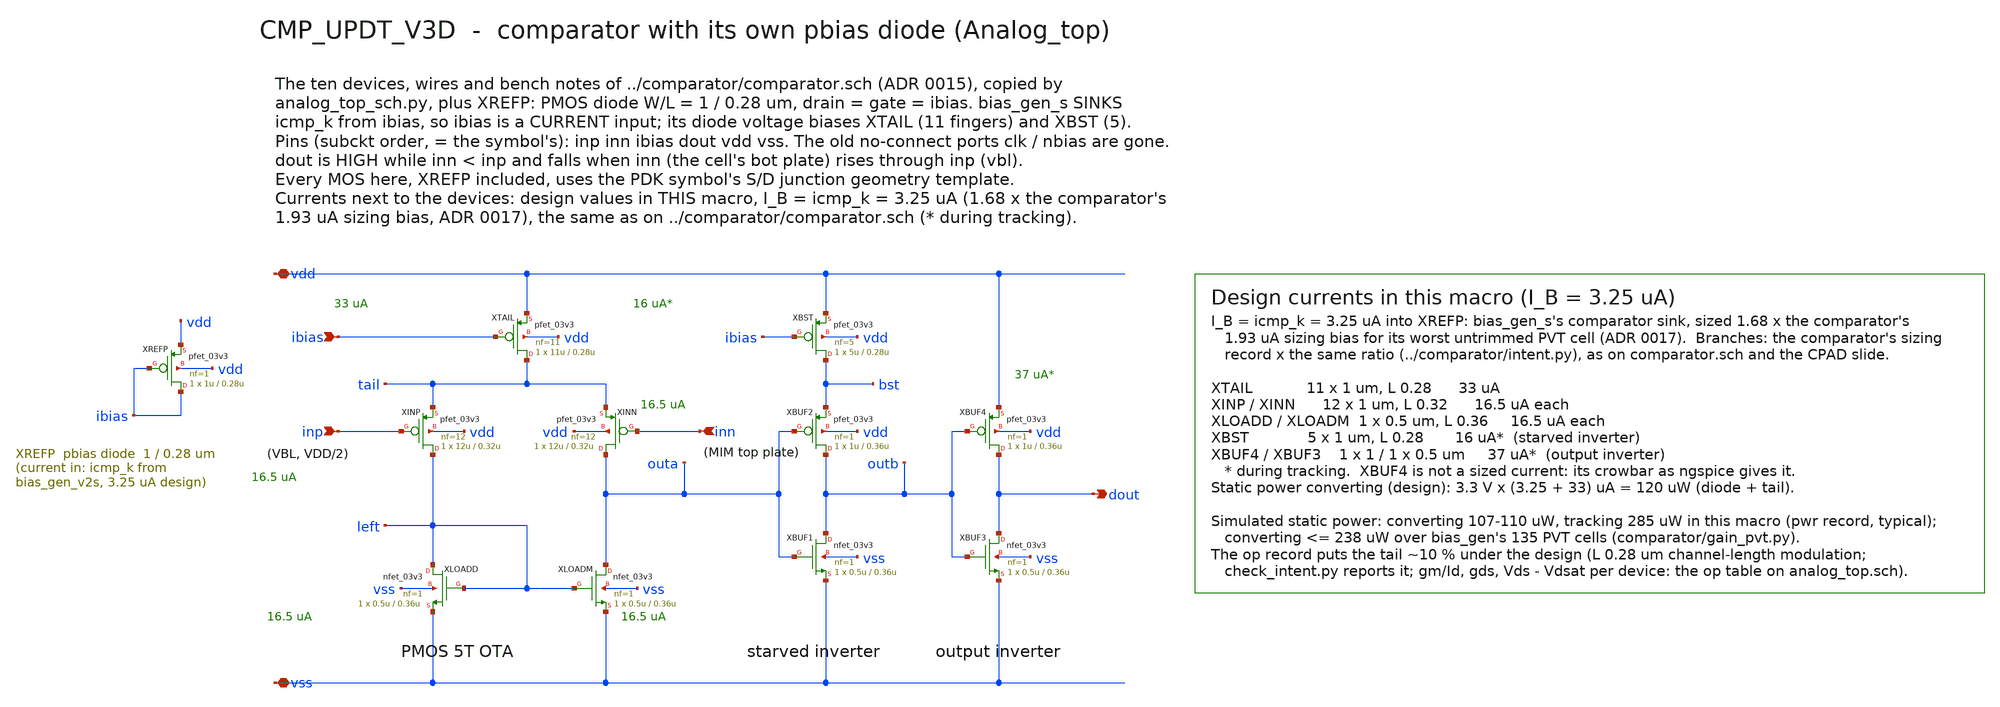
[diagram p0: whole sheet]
** sch_path: mixed_signal/Analog_top/comparator_d.sch
**.subckt comparator_d vdd vss ibias inp inn dout
*.iopin vdd
*.iopin vss
*.ipin ibias
*.ipin inp
*.ipin inn
*.opin dout
XTAIL tail ibias vdd vdd pfet_03v3 L=0.28u W=11u nf=11 ad='int((nf+1)/2) * W/nf * 0.18u' as='int((nf+2)/2) * W/nf * 0.18u'
+ pd='2*int((nf+1)/2) * (W/nf + 0.18u)' ps='2*int((nf+2)/2) * (W/nf + 0.18u)' nrd='0.18u / W' nrs='0.18u / W'
+ sa=0 sb=0 sd=0 m=1
XINP left inp tail vdd pfet_03v3 L=0.32u W=12u nf=12 ad='int((nf+1)/2) * W/nf * 0.18u' as='int((nf+2)/2) * W/nf * 0.18u'
+ pd='2*int((nf+1)/2) * (W/nf + 0.18u)' ps='2*int((nf+2)/2) * (W/nf + 0.18u)' nrd='0.18u / W' nrs='0.18u / W'
+ sa=0 sb=0 sd=0 m=1
XINN outa inn tail vdd pfet_03v3 L=0.32u W=12u nf=12 ad='int((nf+1)/2) * W/nf * 0.18u' as='int((nf+2)/2) * W/nf * 0.18u'
+ pd='2*int((nf+1)/2) * (W/nf + 0.18u)' ps='2*int((nf+2)/2) * (W/nf + 0.18u)' nrd='0.18u / W' nrs='0.18u / W'
+ sa=0 sb=0 sd=0 m=1
XLOADD left left vss vss nfet_03v3 L=0.36u W=0.5u nf=1 ad='int((nf+1)/2) * W/nf * 0.18u' as='int((nf+2)/2) * W/nf * 0.18u'
+ pd='2*int((nf+1)/2) * (W/nf + 0.18u)' ps='2*int((nf+2)/2) * (W/nf + 0.18u)' nrd='0.18u / W' nrs='0.18u / W'
+ sa=0 sb=0 sd=0 m=1
XLOADM outa left vss vss nfet_03v3 L=0.36u W=0.5u nf=1 ad='int((nf+1)/2) * W/nf * 0.18u' as='int((nf+2)/2) * W/nf * 0.18u'
+ pd='2*int((nf+1)/2) * (W/nf + 0.18u)' ps='2*int((nf+2)/2) * (W/nf + 0.18u)' nrd='0.18u / W' nrs='0.18u / W'
+ sa=0 sb=0 sd=0 m=1
XBST bst ibias vdd vdd pfet_03v3 L=0.28u W=5u nf=5 ad='int((nf+1)/2) * W/nf * 0.18u' as='int((nf+2)/2) * W/nf * 0.18u'
+ pd='2*int((nf+1)/2) * (W/nf + 0.18u)' ps='2*int((nf+2)/2) * (W/nf + 0.18u)' nrd='0.18u / W' nrs='0.18u / W'
+ sa=0 sb=0 sd=0 m=1
XBUF2 outb outa bst vdd pfet_03v3 L=0.36u W=1u nf=1 ad='int((nf+1)/2) * W/nf * 0.18u' as='int((nf+2)/2) * W/nf * 0.18u'
+ pd='2*int((nf+1)/2) * (W/nf + 0.18u)' ps='2*int((nf+2)/2) * (W/nf + 0.18u)' nrd='0.18u / W' nrs='0.18u / W'
+ sa=0 sb=0 sd=0 m=1
XBUF1 outb outa vss vss nfet_03v3 L=0.36u W=0.5u nf=1 ad='int((nf+1)/2) * W/nf * 0.18u' as='int((nf+2)/2) * W/nf * 0.18u'
+ pd='2*int((nf+1)/2) * (W/nf + 0.18u)' ps='2*int((nf+2)/2) * (W/nf + 0.18u)' nrd='0.18u / W' nrs='0.18u / W'
+ sa=0 sb=0 sd=0 m=1
XBUF4 dout outb vdd vdd pfet_03v3 L=0.36u W=1u nf=1 ad='int((nf+1)/2) * W/nf * 0.18u' as='int((nf+2)/2) * W/nf * 0.18u'
+ pd='2*int((nf+1)/2) * (W/nf + 0.18u)' ps='2*int((nf+2)/2) * (W/nf + 0.18u)' nrd='0.18u / W' nrs='0.18u / W'
+ sa=0 sb=0 sd=0 m=1
XBUF3 dout outb vss vss nfet_03v3 L=0.36u W=0.5u nf=1 ad='int((nf+1)/2) * W/nf * 0.18u' as='int((nf+2)/2) * W/nf * 0.18u'
+ pd='2*int((nf+1)/2) * (W/nf + 0.18u)' ps='2*int((nf+2)/2) * (W/nf + 0.18u)' nrd='0.18u / W' nrs='0.18u / W'
+ sa=0 sb=0 sd=0 m=1
XREFP ibias ibias vdd vdd pfet_03v3 L=0.28u W=1u nf=1 ad='int((nf+1)/2) * W/nf * 0.18u' as='int((nf+2)/2) * W/nf * 0.18u'
+ pd='2*int((nf+1)/2) * (W/nf + 0.18u)' ps='2*int((nf+2)/2) * (W/nf + 0.18u)' nrd='0.18u / W' nrs='0.18u / W'
+ sa=0 sb=0 sd=0 m=1
**.ends
.end
